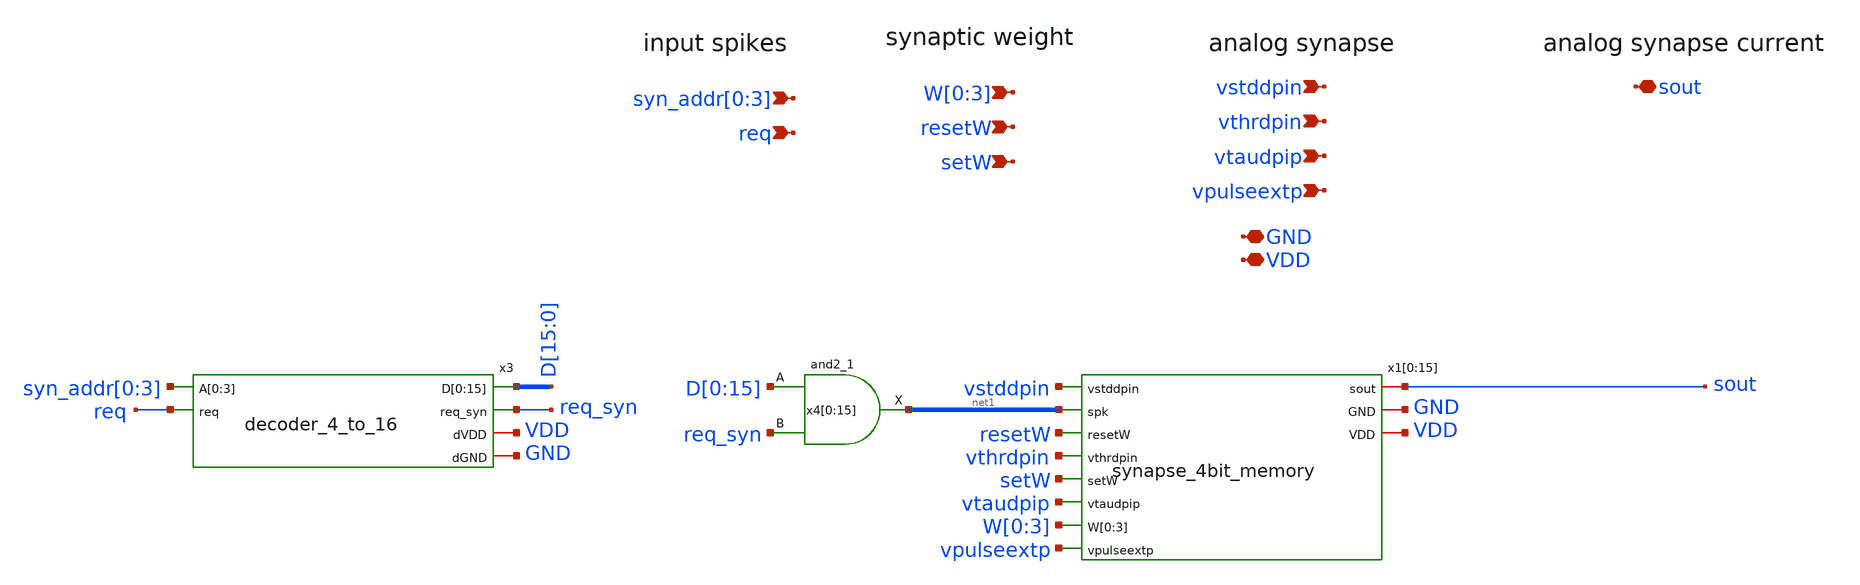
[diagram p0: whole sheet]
** sch_path: design/xschem/synapse_array_programmable_16_to_sout.sch
**.subckt synapse_array_programmable_16_to_sout GND VDD vpulseextp
*+ syn_addr[0],syn_addr[1],syn_addr[2],syn_addr[3] W[0],W[1],W[2],W[3] vthrdpin vtaudpip vstddpin sout setW resetW req
*.iopin GND
*.iopin VDD
*.ipin vpulseextp
*.ipin syn_addr[0],syn_addr[1],syn_addr[2],syn_addr[3]
*.ipin W[0],W[1],W[2],W[3]
*.ipin vthrdpin
*.ipin vtaudpip
*.ipin vstddpin
*.iopin sout
*.ipin setW
*.ipin resetW
*.ipin req
x1[0] sout vstddpin net1[15] resetW vthrdpin setW vtaudpip W[0] W[1] W[2] W[3] vpulseextp GND VDD
+ synapse_4bit_memory
x1[1] sout vstddpin net1[14] resetW vthrdpin setW vtaudpip W[0] W[1] W[2] W[3] vpulseextp GND VDD
+ synapse_4bit_memory
x1[2] sout vstddpin net1[13] resetW vthrdpin setW vtaudpip W[0] W[1] W[2] W[3] vpulseextp GND VDD
+ synapse_4bit_memory
x1[3] sout vstddpin net1[12] resetW vthrdpin setW vtaudpip W[0] W[1] W[2] W[3] vpulseextp GND VDD
+ synapse_4bit_memory
x1[4] sout vstddpin net1[11] resetW vthrdpin setW vtaudpip W[0] W[1] W[2] W[3] vpulseextp GND VDD
+ synapse_4bit_memory
x1[5] sout vstddpin net1[10] resetW vthrdpin setW vtaudpip W[0] W[1] W[2] W[3] vpulseextp GND VDD
+ synapse_4bit_memory
x1[6] sout vstddpin net1[9] resetW vthrdpin setW vtaudpip W[0] W[1] W[2] W[3] vpulseextp GND VDD
+ synapse_4bit_memory
x1[7] sout vstddpin net1[8] resetW vthrdpin setW vtaudpip W[0] W[1] W[2] W[3] vpulseextp GND VDD
+ synapse_4bit_memory
x1[8] sout vstddpin net1[7] resetW vthrdpin setW vtaudpip W[0] W[1] W[2] W[3] vpulseextp GND VDD
+ synapse_4bit_memory
x1[9] sout vstddpin net1[6] resetW vthrdpin setW vtaudpip W[0] W[1] W[2] W[3] vpulseextp GND VDD
+ synapse_4bit_memory
x1[10] sout vstddpin net1[5] resetW vthrdpin setW vtaudpip W[0] W[1] W[2] W[3] vpulseextp GND VDD
+ synapse_4bit_memory
x1[11] sout vstddpin net1[4] resetW vthrdpin setW vtaudpip W[0] W[1] W[2] W[3] vpulseextp GND VDD
+ synapse_4bit_memory
x1[12] sout vstddpin net1[3] resetW vthrdpin setW vtaudpip W[0] W[1] W[2] W[3] vpulseextp GND VDD
+ synapse_4bit_memory
x1[13] sout vstddpin net1[2] resetW vthrdpin setW vtaudpip W[0] W[1] W[2] W[3] vpulseextp GND VDD
+ synapse_4bit_memory
x1[14] sout vstddpin net1[1] resetW vthrdpin setW vtaudpip W[0] W[1] W[2] W[3] vpulseextp GND VDD
+ synapse_4bit_memory
x1[15] sout vstddpin net1[0] resetW vthrdpin setW vtaudpip W[0] W[1] W[2] W[3] vpulseextp GND VDD
+ synapse_4bit_memory
x3 syn_addr[0] syn_addr[1] syn_addr[2] syn_addr[3] D[15] D[14] D[13] D[12] D[11] D[10] D[9] D[8]
+ D[7] D[6] D[5] D[4] D[3] D[2] D[1] D[0] req req_syn VDD GND decoder_4_to_16
x4[0] D[0] req_syn GND GND VDD VDD net1[15] sky130_fd_sc_hd__and2_1
x4[1] D[1] req_syn GND GND VDD VDD net1[14] sky130_fd_sc_hd__and2_1
x4[2] D[2] req_syn GND GND VDD VDD net1[13] sky130_fd_sc_hd__and2_1
x4[3] D[3] req_syn GND GND VDD VDD net1[12] sky130_fd_sc_hd__and2_1
x4[4] D[4] req_syn GND GND VDD VDD net1[11] sky130_fd_sc_hd__and2_1
x4[5] D[5] req_syn GND GND VDD VDD net1[10] sky130_fd_sc_hd__and2_1
x4[6] D[6] req_syn GND GND VDD VDD net1[9] sky130_fd_sc_hd__and2_1
x4[7] D[7] req_syn GND GND VDD VDD net1[8] sky130_fd_sc_hd__and2_1
x4[8] D[8] req_syn GND GND VDD VDD net1[7] sky130_fd_sc_hd__and2_1
x4[9] D[9] req_syn GND GND VDD VDD net1[6] sky130_fd_sc_hd__and2_1
x4[10] D[10] req_syn GND GND VDD VDD net1[5] sky130_fd_sc_hd__and2_1
x4[11] D[11] req_syn GND GND VDD VDD net1[4] sky130_fd_sc_hd__and2_1
x4[12] D[12] req_syn GND GND VDD VDD net1[3] sky130_fd_sc_hd__and2_1
x4[13] D[13] req_syn GND GND VDD VDD net1[2] sky130_fd_sc_hd__and2_1
x4[14] D[14] req_syn GND GND VDD VDD net1[1] sky130_fd_sc_hd__and2_1
x4[15] D[15] req_syn GND GND VDD VDD net1[0] sky130_fd_sc_hd__and2_1
**.ends

* expanding   symbol:  synapse_4bit_memory.sym # of pins=11
** sym_path: design/xschem/synapse_4bit_memory.sym
** sch_path: design/xschem/synapse_4bit_memory.sch
.subckt synapse_4bit_memory sout vstddpin spk resetW vthrdpin setW vtaudpip W[0] W[1] W[2] W[3]
+ vpulseextp GND VDD
*.iopin GND
*.iopin VDD
*.ipin vpulseextp
*.ipin spk
*.ipin vthrdpin
*.ipin vtaudpip
*.ipin vstddpin
*.ipin W[0],W[1],W[2],W[3]
*.ipin setW
*.ipin resetW
*.iopin sout
x1 vpulseextp spk GND spke VDD spike_extender
x3 vtaudpip sout vthrdpin spke vstddpin GND VDD net1[3] net1[2] net1[1] net1[0] dpi_syn_exc_4bit_fc
x2[0] setW W[0] net2 GND GND VDD VDD net1[3] sky130_fd_sc_hd__dfrtp_1
x2[1] setW W[1] net2 GND GND VDD VDD net1[2] sky130_fd_sc_hd__dfrtp_1
x2[2] setW W[2] net2 GND GND VDD VDD net1[1] sky130_fd_sc_hd__dfrtp_1
x2[3] setW W[3] net2 GND GND VDD VDD net1[0] sky130_fd_sc_hd__dfrtp_1
x11 resetW GND GND VDD VDD net2 sky130_fd_sc_hd__inv_1
.ends


* expanding   symbol:  decoder_4_to_16.sym # of pins=6
** sym_path: design/xschem/decoder_4_to_16.sym
** sch_path: design/xschem/decoder_4_to_16.sch
.subckt decoder_4_to_16 A[0] A[1] A[2] A[3] D[0] D[1] D[2] D[3] D[4] D[5] D[6] D[7] D[8] D[9] D[10]
+ D[11] D[12] D[13] D[14] D[15] req req_syn dVDD dGND
*.ipin A[0],A[1],A[2],A[3]
*.ipin req
*.opin D[0],D[1],D[2],D[3],D[4],D[5],D[6],D[7],D[8],D[9],D[10],D[11],D[12],D[13],D[14],D[15]
*.opin req_syn
*.iopin dVDD
*.iopin dGND
x21 req dGND dGND dVDD dVDD net5 sky130_fd_sc_hd__inv_1
x22 net5 dGND dGND dVDD dVDD net6 sky130_fd_sc_hd__inv_1
x23 net6 dGND dGND dVDD dVDD net7 sky130_fd_sc_hd__inv_1
x24 net7 dGND dGND dVDD dVDD req_syn sky130_fd_sc_hd__inv_1
x20 A[3] A[2] A[1] A[0] dGND dGND dVDD dVDD D[15] sky130_fd_sc_hd__and4_1
x19 A[3] A[2] A[1] net4 dGND dGND dVDD dVDD D[14] sky130_fd_sc_hd__and4_1
x18 A[3] A[2] net3 A[0] dGND dGND dVDD dVDD D[13] sky130_fd_sc_hd__and4_1
x17 A[3] A[2] net3 net4 dGND dGND dVDD dVDD D[12] sky130_fd_sc_hd__and4_1
x16 A[3] net2 A[1] A[0] dGND dGND dVDD dVDD D[11] sky130_fd_sc_hd__and4_1
x15 A[3] net2 A[1] net4 dGND dGND dVDD dVDD D[10] sky130_fd_sc_hd__and4_1
x13 A[3] net2 net3 A[0] dGND dGND dVDD dVDD D[9] sky130_fd_sc_hd__and4_1
x4 A[3] net2 net3 net4 dGND dGND dVDD dVDD D[8] sky130_fd_sc_hd__and4_1
x5 net1 A[2] A[1] A[0] dGND dGND dVDD dVDD D[7] sky130_fd_sc_hd__and4_1
x6 net1 A[2] A[1] net4 dGND dGND dVDD dVDD D[6] sky130_fd_sc_hd__and4_1
x8 net1 A[2] net3 net4 dGND dGND dVDD dVDD D[4] sky130_fd_sc_hd__and4_1
x9 net1 net2 A[1] net4 dGND dGND dVDD dVDD D[2] sky130_fd_sc_hd__and4_1
x10 net1 net2 net3 net4 dGND dGND dVDD dVDD D[0] sky130_fd_sc_hd__and4_1
x11 net1 net2 net3 A[0] dGND dGND dVDD dVDD D[1] sky130_fd_sc_hd__and4_1
x12 net1 net2 A[1] A[0] dGND dGND dVDD dVDD D[3] sky130_fd_sc_hd__and4_1
x14 net1 A[2] net3 A[0] dGND dGND dVDD dVDD D[5] sky130_fd_sc_hd__and4_1
x1 A[3] dGND dGND dVDD dVDD net1 sky130_fd_sc_hd__inv_4
x2 A[2] dGND dGND dVDD dVDD net2 sky130_fd_sc_hd__inv_4
x3 A[1] dGND dGND dVDD dVDD net3 sky130_fd_sc_hd__inv_4
x7 A[0] dGND dGND dVDD dVDD net4 sky130_fd_sc_hd__inv_4
.ends


* expanding   symbol:  spike_extender.sym # of pins=5
** sym_path: design/xschem/spike_extender.sym
** sch_path: design/xschem/spike_extender.sch
.subckt spike_extender vpulseextp spk GND spkext VDD
*.iopin GND
*.iopin VDD
*.ipin spk
*.opin spkext
*.ipin vpulseextp
XM1 net1 spk GND GND sky130_fd_pr__nfet_01v8 L=0.15 W=0.65 nf=1 ad='int((nf+1)/2) * W/nf * 0.29' as='int((nf+2)/2) * W/nf * 0.29'
+ pd='2*int((nf+1)/2) * (W/nf + 0.29)' ps='2*int((nf+2)/2) * (W/nf + 0.29)' nrd='0.29 / W' nrs='0.29 / W'
+ sa=0 sb=0 sd=0 mult=1 m=1
XM6 net1 vpulseextp VDD VDD sky130_fd_pr__pfet_01v8 L=2 W=1 nf=1 ad='int((nf+1)/2) * W/nf * 0.29' as='int((nf+2)/2) * W/nf * 0.29'
+ pd='2*int((nf+1)/2) * (W/nf + 0.29)' ps='2*int((nf+2)/2) * (W/nf + 0.29)' nrd='0.29 / W' nrs='0.29 / W'
+ sa=0 sb=0 sd=0 mult=1 m=1
XM5 net3 net2 GND GND sky130_fd_pr__nfet_01v8 L=0.15 W=0.65 nf=1 ad='int((nf+1)/2) * W/nf * 0.29' as='int((nf+2)/2) * W/nf * 0.29'
+ pd='2*int((nf+1)/2) * (W/nf + 0.29)' ps='2*int((nf+2)/2) * (W/nf + 0.29)' nrd='0.29 / W' nrs='0.29 / W'
+ sa=0 sb=0 sd=0 mult=1 m=1
XM8 spkext net3 GND GND sky130_fd_pr__nfet_01v8 L=0.15 W=0.65 nf=1 ad='int((nf+1)/2) * W/nf * 0.29' as='int((nf+2)/2) * W/nf * 0.29'
+ pd='2*int((nf+1)/2) * (W/nf + 0.29)' ps='2*int((nf+2)/2) * (W/nf + 0.29)' nrd='0.29 / W' nrs='0.29 / W'
+ sa=0 sb=0 sd=0 mult=1 m=1
XM4 net3 net2 VDD VDD sky130_fd_pr__pfet_01v8 L=0.15 W=1.0 nf=1 ad='int((nf+1)/2) * W/nf * 0.29' as='int((nf+2)/2) * W/nf * 0.29'
+ pd='2*int((nf+1)/2) * (W/nf + 0.29)' ps='2*int((nf+2)/2) * (W/nf + 0.29)' nrd='0.29 / W' nrs='0.29 / W'
+ sa=0 sb=0 sd=0 mult=1 m=1
XM7 spkext net3 VDD VDD sky130_fd_pr__pfet_01v8 L=0.15 W=1.0 nf=1 ad='int((nf+1)/2) * W/nf * 0.29' as='int((nf+2)/2) * W/nf * 0.29'
+ pd='2*int((nf+1)/2) * (W/nf + 0.29)' ps='2*int((nf+2)/2) * (W/nf + 0.29)' nrd='0.29 / W' nrs='0.29 / W'
+ sa=0 sb=0 sd=0 mult=1 m=1
XM2 net2 net1 GND GND sky130_fd_pr__nfet_01v8 L=0.15 W=0.65 nf=1 ad='int((nf+1)/2) * W/nf * 0.29' as='int((nf+2)/2) * W/nf * 0.29'
+ pd='2*int((nf+1)/2) * (W/nf + 0.29)' ps='2*int((nf+2)/2) * (W/nf + 0.29)' nrd='0.29 / W' nrs='0.29 / W'
+ sa=0 sb=0 sd=0 mult=1 m=1
XM3 net2 net1 VDD VDD sky130_fd_pr__pfet_01v8 L=0.15 W=1.0 nf=1 ad='int((nf+1)/2) * W/nf * 0.29' as='int((nf+2)/2) * W/nf * 0.29'
+ pd='2*int((nf+1)/2) * (W/nf + 0.29)' ps='2*int((nf+2)/2) * (W/nf + 0.29)' nrd='0.29 / W' nrs='0.29 / W'
+ sa=0 sb=0 sd=0 mult=1 m=1
XM9 GND net1 GND GND sky130_fd_pr__nfet_01v8 L=1 W=0.65 nf=1 ad='int((nf+1)/2) * W/nf * 0.29' as='int((nf+2)/2) * W/nf * 0.29'
+ pd='2*int((nf+1)/2) * (W/nf + 0.29)' ps='2*int((nf+2)/2) * (W/nf + 0.29)' nrd='0.29 / W' nrs='0.29 / W'
+ sa=0 sb=0 sd=0 mult=1 m=1
.ends


* expanding   symbol:  dpi_syn_exc_4bit_fc.sym # of pins=8
** sym_path: design/xschem/dpi_syn_exc_4bit_fc.sym
** sch_path: design/xschem/dpi_syn_exc_4bit_fc.sch
.subckt dpi_syn_exc_4bit_fc vtau sout vthn spk vstdn GND VDD weight[0] weight[1] weight[2] weight[3]
*.iopin GND
*.iopin VDD
*.iopin vtau
*.iopin vstdn
*.ipin spk
*.opin sout
*.iopin vthn
*.ipin weight[0],weight[1],weight[2],weight[3]
XM2 net3 spk net1 GND sky130_fd_pr__nfet_01v8 L=0.25 W=0.8 nf=1 ad='int((nf+1)/2) * W/nf * 0.29' as='int((nf+2)/2) * W/nf * 0.29'
+ pd='2*int((nf+1)/2) * (W/nf + 0.29)' ps='2*int((nf+2)/2) * (W/nf + 0.29)' nrd='0.29 / W' nrs='0.29 / W'
+ sa=0 sb=0 sd=0 mult=1 m=1
XC1 vsin VDD sky130_fd_pr__cap_mim_m3_1 W=5 L=5 MF=1 m=1
XM5 vsin vtau VDD VDD sky130_fd_pr__pfet_01v8 L=0.2 W=1.2 nf=1 ad='int((nf+1)/2) * W/nf * 0.29' as='int((nf+2)/2) * W/nf * 0.29'
+ pd='2*int((nf+1)/2) * (W/nf + 0.29)' ps='2*int((nf+2)/2) * (W/nf + 0.29)' nrd='0.29 / W' nrs='0.29 / W'
+ sa=0 sb=0 sd=0 mult=1 m=1
XM6 sout vsin VDD VDD sky130_fd_pr__pfet_01v8 L=0.2 W=1.2 nf=1 ad='int((nf+1)/2) * W/nf * 0.29' as='int((nf+2)/2) * W/nf * 0.29'
+ pd='2*int((nf+1)/2) * (W/nf + 0.29)' ps='2*int((nf+2)/2) * (W/nf + 0.29)' nrd='0.29 / W' nrs='0.29 / W'
+ sa=0 sb=0 sd=0 mult=1 m=1
XM1 net1 vstdn net2 GND sky130_fd_pr__nfet_01v8 L=0.5 W=0.8 nf=1 ad='int((nf+1)/2) * W/nf * 0.29' as='int((nf+2)/2) * W/nf * 0.29'
+ pd='2*int((nf+1)/2) * (W/nf + 0.29)' ps='2*int((nf+2)/2) * (W/nf + 0.29)' nrd='0.29 / W' nrs='0.29 / W'
+ sa=0 sb=0 sd=0 mult=1 m=1
XM4 vsin vsin net3 GND sky130_fd_pr__nfet_01v8 L=0.25 W=0.8 nf=1 ad='int((nf+1)/2) * W/nf * 0.29' as='int((nf+2)/2) * W/nf * 0.29'
+ pd='2*int((nf+1)/2) * (W/nf + 0.29)' ps='2*int((nf+2)/2) * (W/nf + 0.29)' nrd='0.29 / W' nrs='0.29 / W'
+ sa=0 sb=0 sd=0 mult=1 m=1
XM3 VDD vthn net3 GND sky130_fd_pr__nfet_01v8 L=0.25 W=0.8 nf=1 ad='int((nf+1)/2) * W/nf * 0.29' as='int((nf+2)/2) * W/nf * 0.29'
+ pd='2*int((nf+1)/2) * (W/nf + 0.29)' ps='2*int((nf+2)/2) * (W/nf + 0.29)' nrd='0.29 / W' nrs='0.29 / W'
+ sa=0 sb=0 sd=0 mult=1 m=1
XM7 net1 vstdn net4 GND sky130_fd_pr__nfet_01v8 L=2.0 W=0.8 nf=1 ad='int((nf+1)/2) * W/nf * 0.29' as='int((nf+2)/2) * W/nf * 0.29'
+ pd='2*int((nf+1)/2) * (W/nf + 0.29)' ps='2*int((nf+2)/2) * (W/nf + 0.29)' nrd='0.29 / W' nrs='0.29 / W'
+ sa=0 sb=0 sd=0 mult=1 m=1
XM8 net1 vstdn net5 GND sky130_fd_pr__nfet_01v8 L=4.0 W=0.8 nf=1 ad='int((nf+1)/2) * W/nf * 0.29' as='int((nf+2)/2) * W/nf * 0.29'
+ pd='2*int((nf+1)/2) * (W/nf + 0.29)' ps='2*int((nf+2)/2) * (W/nf + 0.29)' nrd='0.29 / W' nrs='0.29 / W'
+ sa=0 sb=0 sd=0 mult=1 m=1
XM9 net1 vstdn net6 GND sky130_fd_pr__nfet_01v8 L=8.0 W=0.8 nf=1 ad='int((nf+1)/2) * W/nf * 0.29' as='int((nf+2)/2) * W/nf * 0.29'
+ pd='2*int((nf+1)/2) * (W/nf + 0.29)' ps='2*int((nf+2)/2) * (W/nf + 0.29)' nrd='0.29 / W' nrs='0.29 / W'
+ sa=0 sb=0 sd=0 mult=1 m=1
XM10 net2 weight[0] GND GND sky130_fd_pr__nfet_01v8 L=0.25 W=0.8 nf=1 ad='int((nf+1)/2) * W/nf * 0.29'
+ as='int((nf+2)/2) * W/nf * 0.29' pd='2*int((nf+1)/2) * (W/nf + 0.29)' ps='2*int((nf+2)/2) * (W/nf + 0.29)'
+ nrd='0.29 / W' nrs='0.29 / W' sa=0 sb=0 sd=0 mult=1 m=1
XM11 net4 weight[1] GND GND sky130_fd_pr__nfet_01v8 L=0.25 W=0.8 nf=1 ad='int((nf+1)/2) * W/nf * 0.29'
+ as='int((nf+2)/2) * W/nf * 0.29' pd='2*int((nf+1)/2) * (W/nf + 0.29)' ps='2*int((nf+2)/2) * (W/nf + 0.29)'
+ nrd='0.29 / W' nrs='0.29 / W' sa=0 sb=0 sd=0 mult=1 m=1
XM12 net5 weight[2] GND GND sky130_fd_pr__nfet_01v8 L=0.25 W=0.8 nf=1 ad='int((nf+1)/2) * W/nf * 0.29'
+ as='int((nf+2)/2) * W/nf * 0.29' pd='2*int((nf+1)/2) * (W/nf + 0.29)' ps='2*int((nf+2)/2) * (W/nf + 0.29)'
+ nrd='0.29 / W' nrs='0.29 / W' sa=0 sb=0 sd=0 mult=1 m=1
XM13 net6 weight[3] GND GND sky130_fd_pr__nfet_01v8 L=0.25 W=0.8 nf=1 ad='int((nf+1)/2) * W/nf * 0.29'
+ as='int((nf+2)/2) * W/nf * 0.29' pd='2*int((nf+1)/2) * (W/nf + 0.29)' ps='2*int((nf+2)/2) * (W/nf + 0.29)'
+ nrd='0.29 / W' nrs='0.29 / W' sa=0 sb=0 sd=0 mult=1 m=1
.ends

.end
